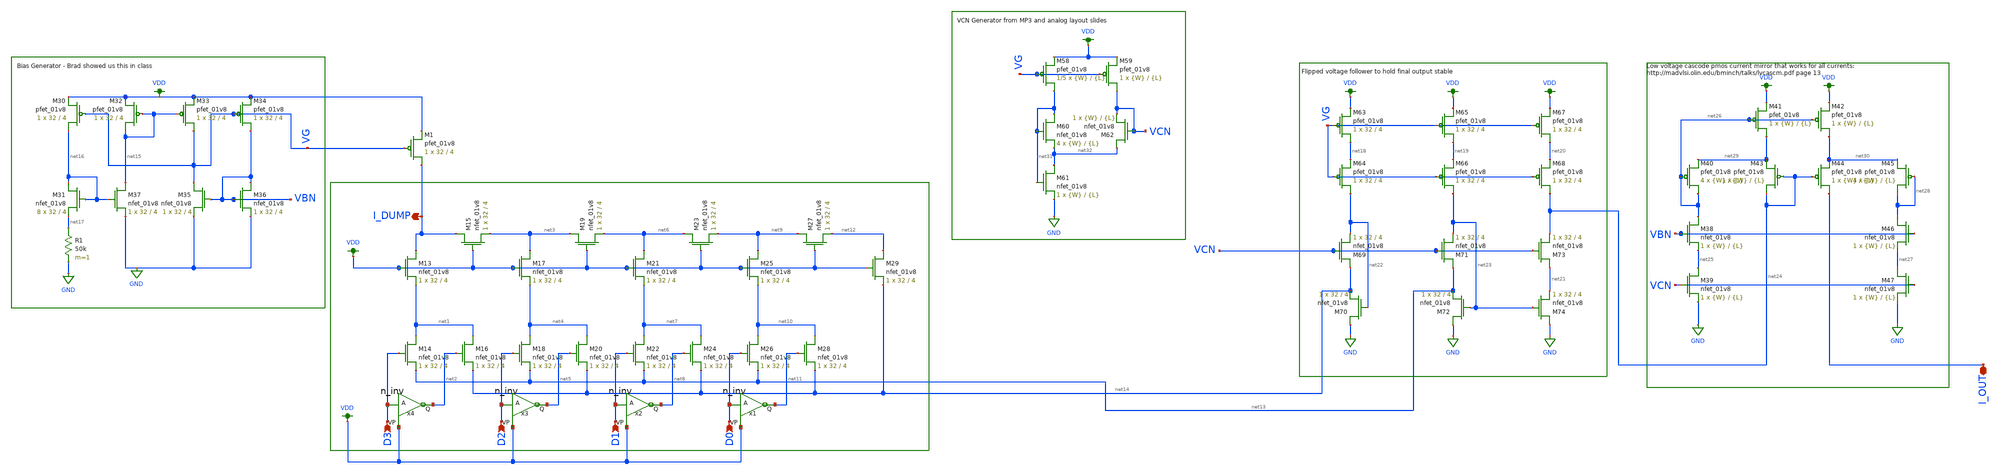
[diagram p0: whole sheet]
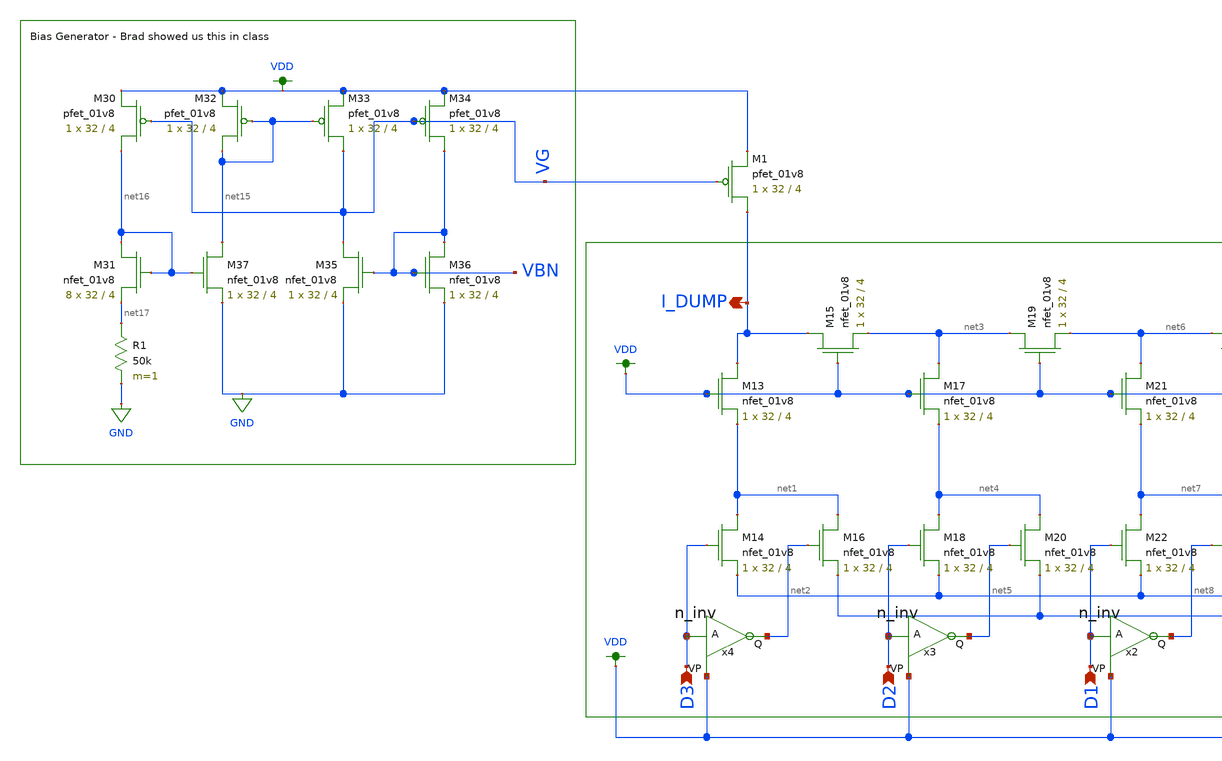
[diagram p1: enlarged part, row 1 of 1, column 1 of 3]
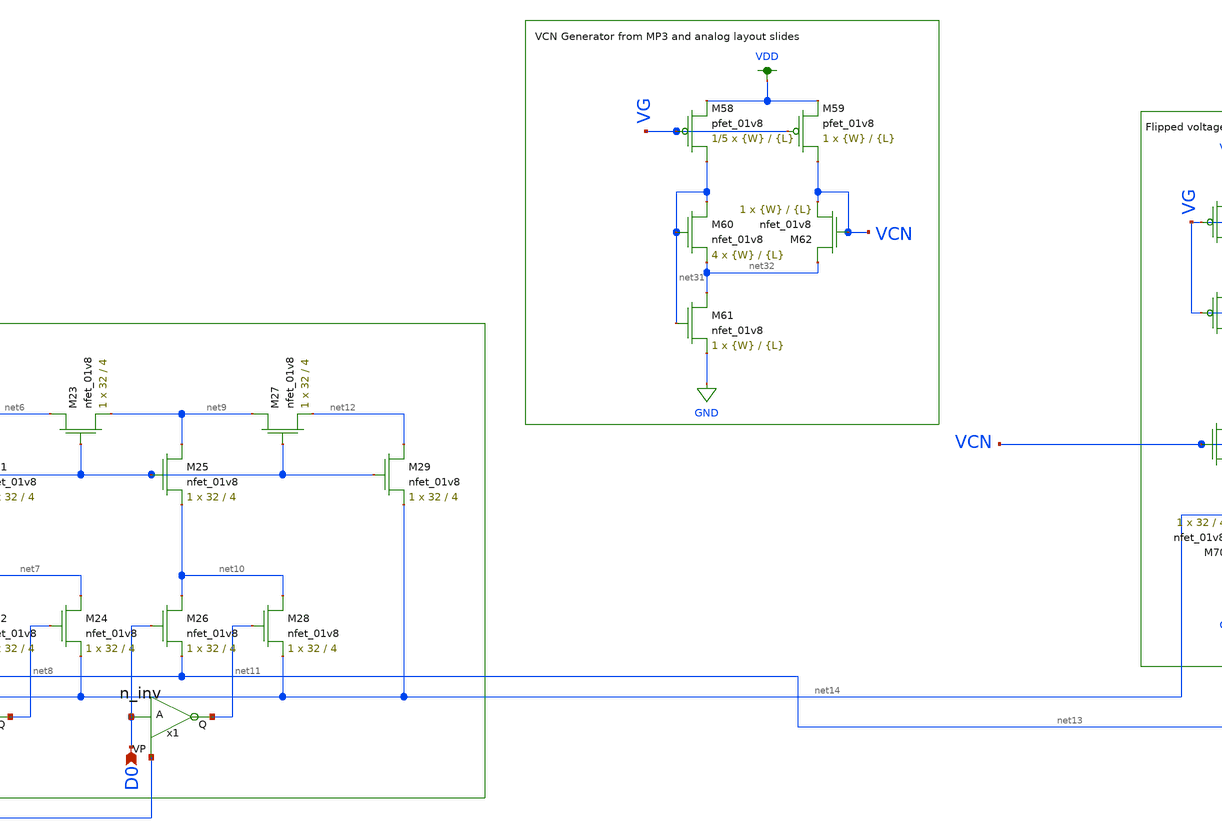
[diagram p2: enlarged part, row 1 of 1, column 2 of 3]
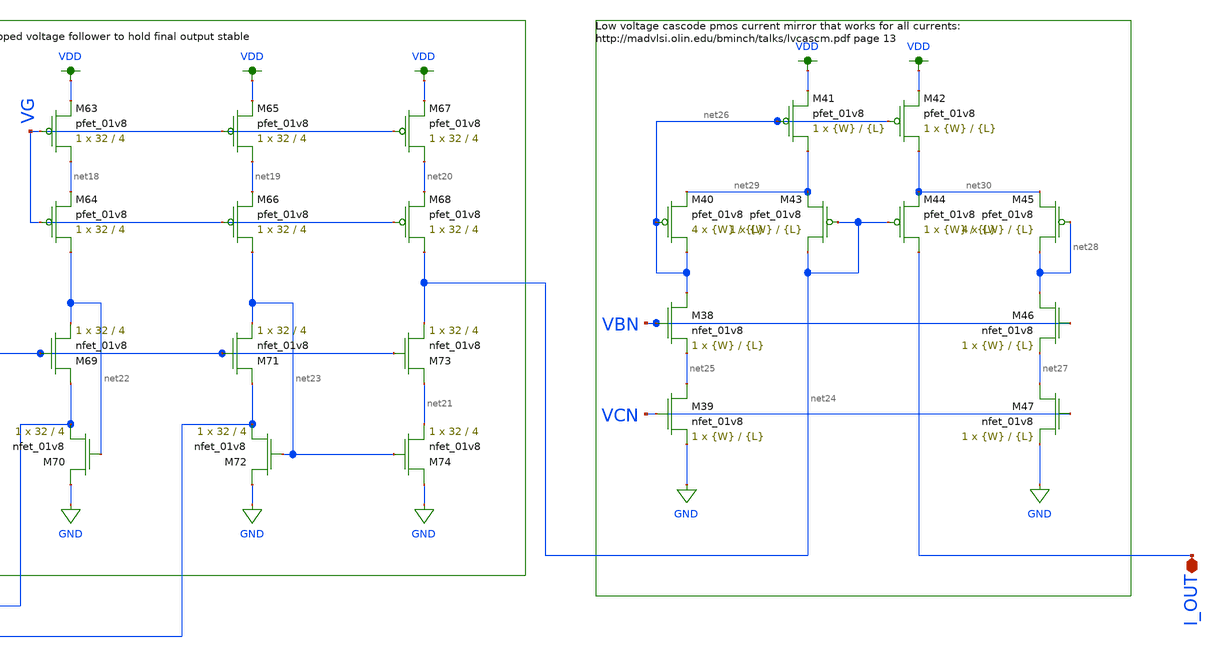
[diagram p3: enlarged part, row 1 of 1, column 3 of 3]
** sch_path: schemas/4BIT_DAC.sch
**.subckt 4BIT_DAC D3 D2 D1 D0 I_OUT I_DUMP
*.ipin D3
*.ipin D2
*.ipin D1
*.ipin D0
*.iopin I_OUT
*.opin I_DUMP
XM13 I_DUMP VDD net1 GND sky130_fd_pr__nfet_01v8 L=4 W=32 nf=1 ad='int((nf+1)/2) * W/nf * 0.29' as='int((nf+2)/2) * W/nf * 0.29'
+ pd='2*int((nf+1)/2) * (W/nf + 0.29)' ps='2*int((nf+2)/2) * (W/nf + 0.29)' nrd='0.29 / W' nrs='0.29 / W'
+ sa=0 sb=0 sd=0 mult=1 m=1
XM14 net1 D3 net13 GND sky130_fd_pr__nfet_01v8 L=4 W=32 nf=1 ad='int((nf+1)/2) * W/nf * 0.29' as='int((nf+2)/2) * W/nf * 0.29'
+ pd='2*int((nf+1)/2) * (W/nf + 0.29)' ps='2*int((nf+2)/2) * (W/nf + 0.29)' nrd='0.29 / W' nrs='0.29 / W'
+ sa=0 sb=0 sd=0 mult=1 m=1
XM15 I_DUMP VDD net3 GND sky130_fd_pr__nfet_01v8 L=4 W=32 nf=1 ad='int((nf+1)/2) * W/nf * 0.29' as='int((nf+2)/2) * W/nf * 0.29'
+ pd='2*int((nf+1)/2) * (W/nf + 0.29)' ps='2*int((nf+2)/2) * (W/nf + 0.29)' nrd='0.29 / W' nrs='0.29 / W'
+ sa=0 sb=0 sd=0 mult=1 m=1
XM16 net1 net2 net14 GND sky130_fd_pr__nfet_01v8 L=4 W=32 nf=1 ad='int((nf+1)/2) * W/nf * 0.29' as='int((nf+2)/2) * W/nf * 0.29'
+ pd='2*int((nf+1)/2) * (W/nf + 0.29)' ps='2*int((nf+2)/2) * (W/nf + 0.29)' nrd='0.29 / W' nrs='0.29 / W'
+ sa=0 sb=0 sd=0 mult=1 m=1
XM17 net3 VDD net4 GND sky130_fd_pr__nfet_01v8 L=4 W=32 nf=1 ad='int((nf+1)/2) * W/nf * 0.29' as='int((nf+2)/2) * W/nf * 0.29'
+ pd='2*int((nf+1)/2) * (W/nf + 0.29)' ps='2*int((nf+2)/2) * (W/nf + 0.29)' nrd='0.29 / W' nrs='0.29 / W'
+ sa=0 sb=0 sd=0 mult=1 m=1
XM18 net4 D2 net13 GND sky130_fd_pr__nfet_01v8 L=4 W=32 nf=1 ad='int((nf+1)/2) * W/nf * 0.29' as='int((nf+2)/2) * W/nf * 0.29'
+ pd='2*int((nf+1)/2) * (W/nf + 0.29)' ps='2*int((nf+2)/2) * (W/nf + 0.29)' nrd='0.29 / W' nrs='0.29 / W'
+ sa=0 sb=0 sd=0 mult=1 m=1
XM19 net3 VDD net6 GND sky130_fd_pr__nfet_01v8 L=4 W=32 nf=1 ad='int((nf+1)/2) * W/nf * 0.29' as='int((nf+2)/2) * W/nf * 0.29'
+ pd='2*int((nf+1)/2) * (W/nf + 0.29)' ps='2*int((nf+2)/2) * (W/nf + 0.29)' nrd='0.29 / W' nrs='0.29 / W'
+ sa=0 sb=0 sd=0 mult=1 m=1
XM20 net4 net5 net14 GND sky130_fd_pr__nfet_01v8 L=4 W=32 nf=1 ad='int((nf+1)/2) * W/nf * 0.29' as='int((nf+2)/2) * W/nf * 0.29'
+ pd='2*int((nf+1)/2) * (W/nf + 0.29)' ps='2*int((nf+2)/2) * (W/nf + 0.29)' nrd='0.29 / W' nrs='0.29 / W'
+ sa=0 sb=0 sd=0 mult=1 m=1
XM21 net6 VDD net7 GND sky130_fd_pr__nfet_01v8 L=4 W=32 nf=1 ad='int((nf+1)/2) * W/nf * 0.29' as='int((nf+2)/2) * W/nf * 0.29'
+ pd='2*int((nf+1)/2) * (W/nf + 0.29)' ps='2*int((nf+2)/2) * (W/nf + 0.29)' nrd='0.29 / W' nrs='0.29 / W'
+ sa=0 sb=0 sd=0 mult=1 m=1
XM22 net7 D1 net13 GND sky130_fd_pr__nfet_01v8 L=4 W=32 nf=1 ad='int((nf+1)/2) * W/nf * 0.29' as='int((nf+2)/2) * W/nf * 0.29'
+ pd='2*int((nf+1)/2) * (W/nf + 0.29)' ps='2*int((nf+2)/2) * (W/nf + 0.29)' nrd='0.29 / W' nrs='0.29 / W'
+ sa=0 sb=0 sd=0 mult=1 m=1
XM23 net6 VDD net9 GND sky130_fd_pr__nfet_01v8 L=4 W=32 nf=1 ad='int((nf+1)/2) * W/nf * 0.29' as='int((nf+2)/2) * W/nf * 0.29'
+ pd='2*int((nf+1)/2) * (W/nf + 0.29)' ps='2*int((nf+2)/2) * (W/nf + 0.29)' nrd='0.29 / W' nrs='0.29 / W'
+ sa=0 sb=0 sd=0 mult=1 m=1
XM24 net7 net8 net14 GND sky130_fd_pr__nfet_01v8 L=4 W=32 nf=1 ad='int((nf+1)/2) * W/nf * 0.29' as='int((nf+2)/2) * W/nf * 0.29'
+ pd='2*int((nf+1)/2) * (W/nf + 0.29)' ps='2*int((nf+2)/2) * (W/nf + 0.29)' nrd='0.29 / W' nrs='0.29 / W'
+ sa=0 sb=0 sd=0 mult=1 m=1
XM25 net9 VDD net10 GND sky130_fd_pr__nfet_01v8 L=4 W=32 nf=1 ad='int((nf+1)/2) * W/nf * 0.29' as='int((nf+2)/2) * W/nf * 0.29'
+ pd='2*int((nf+1)/2) * (W/nf + 0.29)' ps='2*int((nf+2)/2) * (W/nf + 0.29)' nrd='0.29 / W' nrs='0.29 / W'
+ sa=0 sb=0 sd=0 mult=1 m=1
XM26 net10 D0 net13 GND sky130_fd_pr__nfet_01v8 L=4 W=32 nf=1 ad='int((nf+1)/2) * W/nf * 0.29' as='int((nf+2)/2) * W/nf * 0.29'
+ pd='2*int((nf+1)/2) * (W/nf + 0.29)' ps='2*int((nf+2)/2) * (W/nf + 0.29)' nrd='0.29 / W' nrs='0.29 / W'
+ sa=0 sb=0 sd=0 mult=1 m=1
XM27 net9 VDD net12 GND sky130_fd_pr__nfet_01v8 L=4 W=32 nf=1 ad='int((nf+1)/2) * W/nf * 0.29' as='int((nf+2)/2) * W/nf * 0.29'
+ pd='2*int((nf+1)/2) * (W/nf + 0.29)' ps='2*int((nf+2)/2) * (W/nf + 0.29)' nrd='0.29 / W' nrs='0.29 / W'
+ sa=0 sb=0 sd=0 mult=1 m=1
XM28 net10 net11 net14 GND sky130_fd_pr__nfet_01v8 L=4 W=32 nf=1 ad='int((nf+1)/2) * W/nf * 0.29' as='int((nf+2)/2) * W/nf * 0.29'
+ pd='2*int((nf+1)/2) * (W/nf + 0.29)' ps='2*int((nf+2)/2) * (W/nf + 0.29)' nrd='0.29 / W' nrs='0.29 / W'
+ sa=0 sb=0 sd=0 mult=1 m=1
XM29 net12 VDD net14 GND sky130_fd_pr__nfet_01v8 L=4 W=32 nf=1 ad='int((nf+1)/2) * W/nf * 0.29' as='int((nf+2)/2) * W/nf * 0.29'
+ pd='2*int((nf+1)/2) * (W/nf + 0.29)' ps='2*int((nf+2)/2) * (W/nf + 0.29)' nrd='0.29 / W' nrs='0.29 / W'
+ sa=0 sb=0 sd=0 mult=1 m=1
XM30 net16 VG VDD VDD sky130_fd_pr__pfet_01v8 L=4 W=32 nf=1 ad='int((nf+1)/2) * W/nf * 0.29' as='int((nf+2)/2) * W/nf * 0.29'
+ pd='2*int((nf+1)/2) * (W/nf + 0.29)' ps='2*int((nf+2)/2) * (W/nf + 0.29)' nrd='0.29 / W' nrs='0.29 / W'
+ sa=0 sb=0 sd=0 mult=1 m=1
XM31 net16 net16 net17 GND sky130_fd_pr__nfet_01v8 L=4 W=32 nf=1 ad='int((nf+1)/2) * W/nf * 0.29' as='int((nf+2)/2) * W/nf * 0.29'
+ pd='2*int((nf+1)/2) * (W/nf + 0.29)' ps='2*int((nf+2)/2) * (W/nf + 0.29)' nrd='0.29 / W' nrs='0.29 / W'
+ sa=0 sb=0 sd=0 mult=8 m=8
XM32 net15 net15 VDD VDD sky130_fd_pr__pfet_01v8 L=4 W=32 nf=1 ad='int((nf+1)/2) * W/nf * 0.29' as='int((nf+2)/2) * W/nf * 0.29'
+ pd='2*int((nf+1)/2) * (W/nf + 0.29)' ps='2*int((nf+2)/2) * (W/nf + 0.29)' nrd='0.29 / W' nrs='0.29 / W'
+ sa=0 sb=0 sd=0 mult=1 m=1
XM33 VG net15 VDD VDD sky130_fd_pr__pfet_01v8 L=4 W=32 nf=1 ad='int((nf+1)/2) * W/nf * 0.29' as='int((nf+2)/2) * W/nf * 0.29'
+ pd='2*int((nf+1)/2) * (W/nf + 0.29)' ps='2*int((nf+2)/2) * (W/nf + 0.29)' nrd='0.29 / W' nrs='0.29 / W'
+ sa=0 sb=0 sd=0 mult=1 m=1
XM34 VBN VG VDD VDD sky130_fd_pr__pfet_01v8 L=4 W=32 nf=1 ad='int((nf+1)/2) * W/nf * 0.29' as='int((nf+2)/2) * W/nf * 0.29'
+ pd='2*int((nf+1)/2) * (W/nf + 0.29)' ps='2*int((nf+2)/2) * (W/nf + 0.29)' nrd='0.29 / W' nrs='0.29 / W'
+ sa=0 sb=0 sd=0 mult=1 m=1
XM35 VG VBN GND GND sky130_fd_pr__nfet_01v8 L=4 W=32 nf=1 ad='int((nf+1)/2) * W/nf * 0.29' as='int((nf+2)/2) * W/nf * 0.29'
+ pd='2*int((nf+1)/2) * (W/nf + 0.29)' ps='2*int((nf+2)/2) * (W/nf + 0.29)' nrd='0.29 / W' nrs='0.29 / W'
+ sa=0 sb=0 sd=0 mult=1 m=1
XM36 VBN VBN GND GND sky130_fd_pr__nfet_01v8 L=4 W=32 nf=1 ad='int((nf+1)/2) * W/nf * 0.29' as='int((nf+2)/2) * W/nf * 0.29'
+ pd='2*int((nf+1)/2) * (W/nf + 0.29)' ps='2*int((nf+2)/2) * (W/nf + 0.29)' nrd='0.29 / W' nrs='0.29 / W'
+ sa=0 sb=0 sd=0 mult=1 m=1
XM37 net15 net16 GND GND sky130_fd_pr__nfet_01v8 L=4 W=32 nf=1 ad='int((nf+1)/2) * W/nf * 0.29' as='int((nf+2)/2) * W/nf * 0.29'
+ pd='2*int((nf+1)/2) * (W/nf + 0.29)' ps='2*int((nf+2)/2) * (W/nf + 0.29)' nrd='0.29 / W' nrs='0.29 / W'
+ sa=0 sb=0 sd=0 mult=1 m=1
R1 net17 GND 50k m=1
XM63 net18 VG VDD VDD sky130_fd_pr__pfet_01v8 L=4 W=32 nf=1 ad='int((nf+1)/2) * W/nf * 0.29' as='int((nf+2)/2) * W/nf * 0.29'
+ pd='2*int((nf+1)/2) * (W/nf + 0.29)' ps='2*int((nf+2)/2) * (W/nf + 0.29)' nrd='0.29 / W' nrs='0.29 / W'
+ sa=0 sb=0 sd=0 mult=1 m=1
XM64 net22 VG net18 VDD sky130_fd_pr__pfet_01v8 L=4 W=32 nf=1 ad='int((nf+1)/2) * W/nf * 0.29' as='int((nf+2)/2) * W/nf * 0.29'
+ pd='2*int((nf+1)/2) * (W/nf + 0.29)' ps='2*int((nf+2)/2) * (W/nf + 0.29)' nrd='0.29 / W' nrs='0.29 / W'
+ sa=0 sb=0 sd=0 mult=1 m=1
XM65 net19 VG VDD VDD sky130_fd_pr__pfet_01v8 L=4 W=32 nf=1 ad='int((nf+1)/2) * W/nf * 0.29' as='int((nf+2)/2) * W/nf * 0.29'
+ pd='2*int((nf+1)/2) * (W/nf + 0.29)' ps='2*int((nf+2)/2) * (W/nf + 0.29)' nrd='0.29 / W' nrs='0.29 / W'
+ sa=0 sb=0 sd=0 mult=1 m=1
XM66 net23 VG net19 VDD sky130_fd_pr__pfet_01v8 L=4 W=32 nf=1 ad='int((nf+1)/2) * W/nf * 0.29' as='int((nf+2)/2) * W/nf * 0.29'
+ pd='2*int((nf+1)/2) * (W/nf + 0.29)' ps='2*int((nf+2)/2) * (W/nf + 0.29)' nrd='0.29 / W' nrs='0.29 / W'
+ sa=0 sb=0 sd=0 mult=1 m=1
XM67 net20 VG VDD VDD sky130_fd_pr__pfet_01v8 L=4 W=32 nf=1 ad='int((nf+1)/2) * W/nf * 0.29' as='int((nf+2)/2) * W/nf * 0.29'
+ pd='2*int((nf+1)/2) * (W/nf + 0.29)' ps='2*int((nf+2)/2) * (W/nf + 0.29)' nrd='0.29 / W' nrs='0.29 / W'
+ sa=0 sb=0 sd=0 mult=1 m=1
XM68 net24 VG net20 VDD sky130_fd_pr__pfet_01v8 L=4 W=32 nf=1 ad='int((nf+1)/2) * W/nf * 0.29' as='int((nf+2)/2) * W/nf * 0.29'
+ pd='2*int((nf+1)/2) * (W/nf + 0.29)' ps='2*int((nf+2)/2) * (W/nf + 0.29)' nrd='0.29 / W' nrs='0.29 / W'
+ sa=0 sb=0 sd=0 mult=1 m=1
XM69 net14 VCN net22 GND sky130_fd_pr__nfet_01v8 L=4 W=32 nf=1 ad='int((nf+1)/2) * W/nf * 0.29' as='int((nf+2)/2) * W/nf * 0.29'
+ pd='2*int((nf+1)/2) * (W/nf + 0.29)' ps='2*int((nf+2)/2) * (W/nf + 0.29)' nrd='0.29 / W' nrs='0.29 / W'
+ sa=0 sb=0 sd=0 mult=1 m=1
XM70 GND net22 net14 GND sky130_fd_pr__nfet_01v8 L=4 W=32 nf=1 ad='int((nf+1)/2) * W/nf * 0.29' as='int((nf+2)/2) * W/nf * 0.29'
+ pd='2*int((nf+1)/2) * (W/nf + 0.29)' ps='2*int((nf+2)/2) * (W/nf + 0.29)' nrd='0.29 / W' nrs='0.29 / W'
+ sa=0 sb=0 sd=0 mult=1 m=1
XM71 net13 VCN net23 GND sky130_fd_pr__nfet_01v8 L=4 W=32 nf=1 ad='int((nf+1)/2) * W/nf * 0.29' as='int((nf+2)/2) * W/nf * 0.29'
+ pd='2*int((nf+1)/2) * (W/nf + 0.29)' ps='2*int((nf+2)/2) * (W/nf + 0.29)' nrd='0.29 / W' nrs='0.29 / W'
+ sa=0 sb=0 sd=0 mult=1 m=1
XM72 GND net23 net13 GND sky130_fd_pr__nfet_01v8 L=4 W=32 nf=1 ad='int((nf+1)/2) * W/nf * 0.29' as='int((nf+2)/2) * W/nf * 0.29'
+ pd='2*int((nf+1)/2) * (W/nf + 0.29)' ps='2*int((nf+2)/2) * (W/nf + 0.29)' nrd='0.29 / W' nrs='0.29 / W'
+ sa=0 sb=0 sd=0 mult=1 m=1
XM73 net21 VCN net24 GND sky130_fd_pr__nfet_01v8 L=4 W=32 nf=1 ad='int((nf+1)/2) * W/nf * 0.29' as='int((nf+2)/2) * W/nf * 0.29'
+ pd='2*int((nf+1)/2) * (W/nf + 0.29)' ps='2*int((nf+2)/2) * (W/nf + 0.29)' nrd='0.29 / W' nrs='0.29 / W'
+ sa=0 sb=0 sd=0 mult=1 m=1
XM74 GND net23 net21 GND sky130_fd_pr__nfet_01v8 L=4 W=32 nf=1 ad='int((nf+1)/2) * W/nf * 0.29' as='int((nf+2)/2) * W/nf * 0.29'
+ pd='2*int((nf+1)/2) * (W/nf + 0.29)' ps='2*int((nf+2)/2) * (W/nf + 0.29)' nrd='0.29 / W' nrs='0.29 / W'
+ sa=0 sb=0 sd=0 mult=1 m=1
XM1 I_DUMP VG VDD VDD sky130_fd_pr__pfet_01v8 L=4 W=32 nf=1 ad='int((nf+1)/2) * W/nf * 0.29' as='int((nf+2)/2) * W/nf * 0.29'
+ pd='2*int((nf+1)/2) * (W/nf + 0.29)' ps='2*int((nf+2)/2) * (W/nf + 0.29)' nrd='0.29 / W' nrs='0.29 / W'
+ sa=0 sb=0 sd=0 mult=1 m=1
x1 VDD net11 D0 n_inv
x2 VDD net8 D1 n_inv
x3 VDD net5 D2 n_inv
x4 VDD net2 D3 n_inv
XM38 net26 VBN net25 GND sky130_fd_pr__nfet_01v8 L={L} W={W} nf=1 ad='int((nf+1)/2) * W/nf * 0.29' as='int((nf+2)/2) * W/nf * 0.29'
+ pd='2*int((nf+1)/2) * (W/nf + 0.29)' ps='2*int((nf+2)/2) * (W/nf + 0.29)' nrd='0.29 / W' nrs='0.29 / W'
+ sa=0 sb=0 sd=0 mult=1 m=1
XM39 net25 VCN GND GND sky130_fd_pr__nfet_01v8 L={L} W={W} nf=1 ad='int((nf+1)/2) * W/nf * 0.29' as='int((nf+2)/2) * W/nf * 0.29'
+ pd='2*int((nf+1)/2) * (W/nf + 0.29)' ps='2*int((nf+2)/2) * (W/nf + 0.29)' nrd='0.29 / W' nrs='0.29 / W'
+ sa=0 sb=0 sd=0 mult=1 m=1
XM40 net26 net26 net29 VDD sky130_fd_pr__pfet_01v8 L={L} W={W} nf=1 ad='int((nf+1)/2) * W/nf * 0.29'
+ as='int((nf+2)/2) * W/nf * 0.29' pd='2*int((nf+1)/2) * (W/nf + 0.29)' ps='2*int((nf+2)/2) * (W/nf + 0.29)'
+ nrd='0.29 / W' nrs='0.29 / W' sa=0 sb=0 sd=0 mult=4 m=4
XM41 net29 net26 VDD VDD sky130_fd_pr__pfet_01v8 L={L} W={W} nf=1 ad='int((nf+1)/2) * W/nf * 0.29' as='int((nf+2)/2) * W/nf * 0.29'
+ pd='2*int((nf+1)/2) * (W/nf + 0.29)' ps='2*int((nf+2)/2) * (W/nf + 0.29)' nrd='0.29 / W' nrs='0.29 / W'
+ sa=0 sb=0 sd=0 mult=1 m=1
XM42 net30 net26 VDD VDD sky130_fd_pr__pfet_01v8 L={L} W={W} nf=1 ad='int((nf+1)/2) * W/nf * 0.29' as='int((nf+2)/2) * W/nf * 0.29'
+ pd='2*int((nf+1)/2) * (W/nf + 0.29)' ps='2*int((nf+2)/2) * (W/nf + 0.29)' nrd='0.29 / W' nrs='0.29 / W'
+ sa=0 sb=0 sd=0 mult=1 m=1
XM43 net24 net24 net29 VDD sky130_fd_pr__pfet_01v8 L={L} W={W} nf=1 ad='int((nf+1)/2) * W/nf * 0.29'
+ as='int((nf+2)/2) * W/nf * 0.29' pd='2*int((nf+1)/2) * (W/nf + 0.29)' ps='2*int((nf+2)/2) * (W/nf + 0.29)'
+ nrd='0.29 / W' nrs='0.29 / W' sa=0 sb=0 sd=0 mult=1 m=1
XM44 I_OUT net24 net30 VDD sky130_fd_pr__pfet_01v8 L={L} W={W} nf=1 ad='int((nf+1)/2) * W/nf * 0.29'
+ as='int((nf+2)/2) * W/nf * 0.29' pd='2*int((nf+1)/2) * (W/nf + 0.29)' ps='2*int((nf+2)/2) * (W/nf + 0.29)'
+ nrd='0.29 / W' nrs='0.29 / W' sa=0 sb=0 sd=0 mult=1 m=1
XM45 net28 net28 net30 VDD sky130_fd_pr__pfet_01v8 L={L} W={W} nf=1 ad='int((nf+1)/2) * W/nf * 0.29'
+ as='int((nf+2)/2) * W/nf * 0.29' pd='2*int((nf+1)/2) * (W/nf + 0.29)' ps='2*int((nf+2)/2) * (W/nf + 0.29)'
+ nrd='0.29 / W' nrs='0.29 / W' sa=0 sb=0 sd=0 mult=4 m=4
XM46 net28 VBN net27 GND sky130_fd_pr__nfet_01v8 L={L} W={W} nf=1 ad='int((nf+1)/2) * W/nf * 0.29' as='int((nf+2)/2) * W/nf * 0.29'
+ pd='2*int((nf+1)/2) * (W/nf + 0.29)' ps='2*int((nf+2)/2) * (W/nf + 0.29)' nrd='0.29 / W' nrs='0.29 / W'
+ sa=0 sb=0 sd=0 mult=1 m=1
XM47 net27 VCN GND GND sky130_fd_pr__nfet_01v8 L={L} W={W} nf=1 ad='int((nf+1)/2) * W/nf * 0.29' as='int((nf+2)/2) * W/nf * 0.29'
+ pd='2*int((nf+1)/2) * (W/nf + 0.29)' ps='2*int((nf+2)/2) * (W/nf + 0.29)' nrd='0.29 / W' nrs='0.29 / W'
+ sa=0 sb=0 sd=0 mult=1 m=1
XM58 net31 VG VDD VDD sky130_fd_pr__pfet_01v8 L={L} W={W} nf=1 ad='int((nf+1)/2) * W/nf * 0.29' as='int((nf+2)/2) * W/nf * 0.29'
+ pd='2*int((nf+1)/2) * (W/nf + 0.29)' ps='2*int((nf+2)/2) * (W/nf + 0.29)' nrd='0.29 / W' nrs='0.29 / W'
+ sa=0 sb=0 sd=0 mult=1/5 m=1/5
XM59 VCN VG VDD VDD sky130_fd_pr__pfet_01v8 L={L} W={W} nf=1 ad='int((nf+1)/2) * W/nf * 0.29' as='int((nf+2)/2) * W/nf * 0.29'
+ pd='2*int((nf+1)/2) * (W/nf + 0.29)' ps='2*int((nf+2)/2) * (W/nf + 0.29)' nrd='0.29 / W' nrs='0.29 / W'
+ sa=0 sb=0 sd=0 mult=1 m=1
XM60 net31 net31 net32 GND sky130_fd_pr__nfet_01v8 L={L} W={W} nf=1 ad='int((nf+1)/2) * W/nf * 0.29'
+ as='int((nf+2)/2) * W/nf * 0.29' pd='2*int((nf+1)/2) * (W/nf + 0.29)' ps='2*int((nf+2)/2) * (W/nf + 0.29)'
+ nrd='0.29 / W' nrs='0.29 / W' sa=0 sb=0 sd=0 mult=4 m=4
XM61 net32 net31 GND GND sky130_fd_pr__nfet_01v8 L={L} W={W} nf=1 ad='int((nf+1)/2) * W/nf * 0.29' as='int((nf+2)/2) * W/nf * 0.29'
+ pd='2*int((nf+1)/2) * (W/nf + 0.29)' ps='2*int((nf+2)/2) * (W/nf + 0.29)' nrd='0.29 / W' nrs='0.29 / W'
+ sa=0 sb=0 sd=0 mult=1 m=1
XM62 net32 VCN VCN GND sky130_fd_pr__nfet_01v8 L={L} W={W} nf=1 ad='int((nf+1)/2) * W/nf * 0.29' as='int((nf+2)/2) * W/nf * 0.29'
+ pd='2*int((nf+1)/2) * (W/nf + 0.29)' ps='2*int((nf+2)/2) * (W/nf + 0.29)' nrd='0.29 / W' nrs='0.29 / W'
+ sa=0 sb=0 sd=0 mult=1 m=1
**.ends

* expanding   symbol:  /home/lxbtlr/DTILO/schemas/n_inv.sym # of pins=3
** sym_path: schemas/n_inv.sym
** sch_path: schemas/n_inv.sch
.subckt n_inv VP Q A
*.ipin A
*.ipin VP
*.opin Q
XM1 Q A GND GND sky130_fd_pr__nfet_01v8 L={invL} W={invW} nf=1 ad='int((nf+1)/2) * W/nf * 0.29' as='int((nf+2)/2) * W/nf * 0.29'
+ pd='2*int((nf+1)/2) * (W/nf + 0.29)' ps='2*int((nf+2)/2) * (W/nf + 0.29)' nrd='0.29 / W' nrs='0.29 / W'
+ sa=0 sb=0 sd=0 mult=1 m=1
XM2 Q A VP VDD sky130_fd_pr__pfet_01v8 L={invL} W={invW} nf=1 ad='int((nf+1)/2) * W/nf * 0.29' as='int((nf+2)/2) * W/nf * 0.29'
+ pd='2*int((nf+1)/2) * (W/nf + 0.29)' ps='2*int((nf+2)/2) * (W/nf + 0.29)' nrd='0.29 / W' nrs='0.29 / W'
+ sa=0 sb=0 sd=0 mult=1 m=1
.ends

.GLOBAL GND
.GLOBAL VDD
.end
